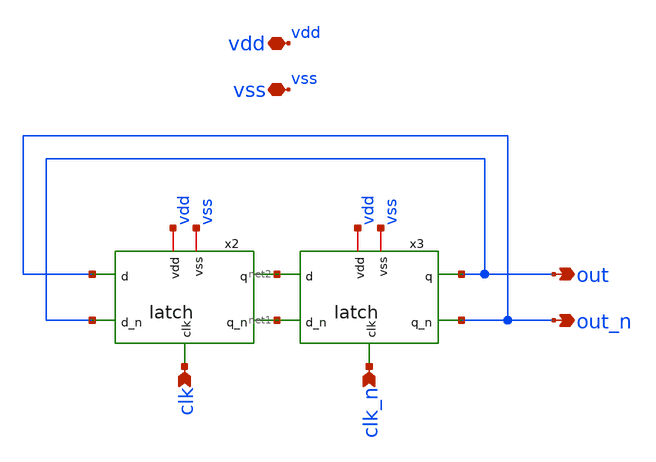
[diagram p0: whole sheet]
** sch_path: xschem/clkdiv2.sch
**.subckt clkdiv2 vdd out vss clk out_n clk_n
*.iopin vdd
*.opin out
*.iopin vss
*.ipin clk
*.opin out_n
*.ipin clk_n
x2 vdd vss net1 net2 out_n out clk latch
x3 vdd vss out_n out net2 net1 clk_n latch
**.ends

* expanding   symbol:  latch.sym # of pins=7
** sym_path: xschem/latch.sym
** sch_path: xschem/latch.sch
.subckt latch vdd vss q_n q d d_n clk
*.iopin vdd
*.ipin d
*.opin q
*.iopin vss
*.ipin d_n
*.opin q_n
*.ipin clk
XM11 q_n q vdd vdd sky130_fd_pr__pfet_01v8 L=0.15 W=2 nf=1 ad='int((nf+1)/2) * W/nf * 0.29' as='int((nf+2)/2) * W/nf * 0.29'
+ pd='2*int((nf+1)/2) * (W/nf + 0.29)' ps='2*int((nf+2)/2) * (W/nf + 0.29)' nrd='0.29 / W' nrs='0.29 / W'
+ sa=0 sb=0 sd=0 mult=1 m=1
XM12 q q_n vdd vdd sky130_fd_pr__pfet_01v8 L=0.15 W=2 nf=1 ad='int((nf+1)/2) * W/nf * 0.29' as='int((nf+2)/2) * W/nf * 0.29'
+ pd='2*int((nf+1)/2) * (W/nf + 0.29)' ps='2*int((nf+2)/2) * (W/nf + 0.29)' nrd='0.29 / W' nrs='0.29 / W'
+ sa=0 sb=0 sd=0 mult=1 m=1
XM13 q_n d net1 vss sky130_fd_pr__nfet_01v8 L=0.15 W=1 nf=1 ad='int((nf+1)/2) * W/nf * 0.29' as='int((nf+2)/2) * W/nf * 0.29'
+ pd='2*int((nf+1)/2) * (W/nf + 0.29)' ps='2*int((nf+2)/2) * (W/nf + 0.29)' nrd='0.29 / W' nrs='0.29 / W'
+ sa=0 sb=0 sd=0 mult=1 m=1
XM14 q d_n net1 vss sky130_fd_pr__nfet_01v8 L=0.15 W=1 nf=1 ad='int((nf+1)/2) * W/nf * 0.29' as='int((nf+2)/2) * W/nf * 0.29'
+ pd='2*int((nf+1)/2) * (W/nf + 0.29)' ps='2*int((nf+2)/2) * (W/nf + 0.29)' nrd='0.29 / W' nrs='0.29 / W'
+ sa=0 sb=0 sd=0 mult=1 m=1
XM15 net1 clk vss vss sky130_fd_pr__nfet_01v8 L=0.15 W=2 nf=1 ad='int((nf+1)/2) * W/nf * 0.29' as='int((nf+2)/2) * W/nf * 0.29'
+ pd='2*int((nf+1)/2) * (W/nf + 0.29)' ps='2*int((nf+2)/2) * (W/nf + 0.29)' nrd='0.29 / W' nrs='0.29 / W'
+ sa=0 sb=0 sd=0 mult=1 m=1
.ends

.end
